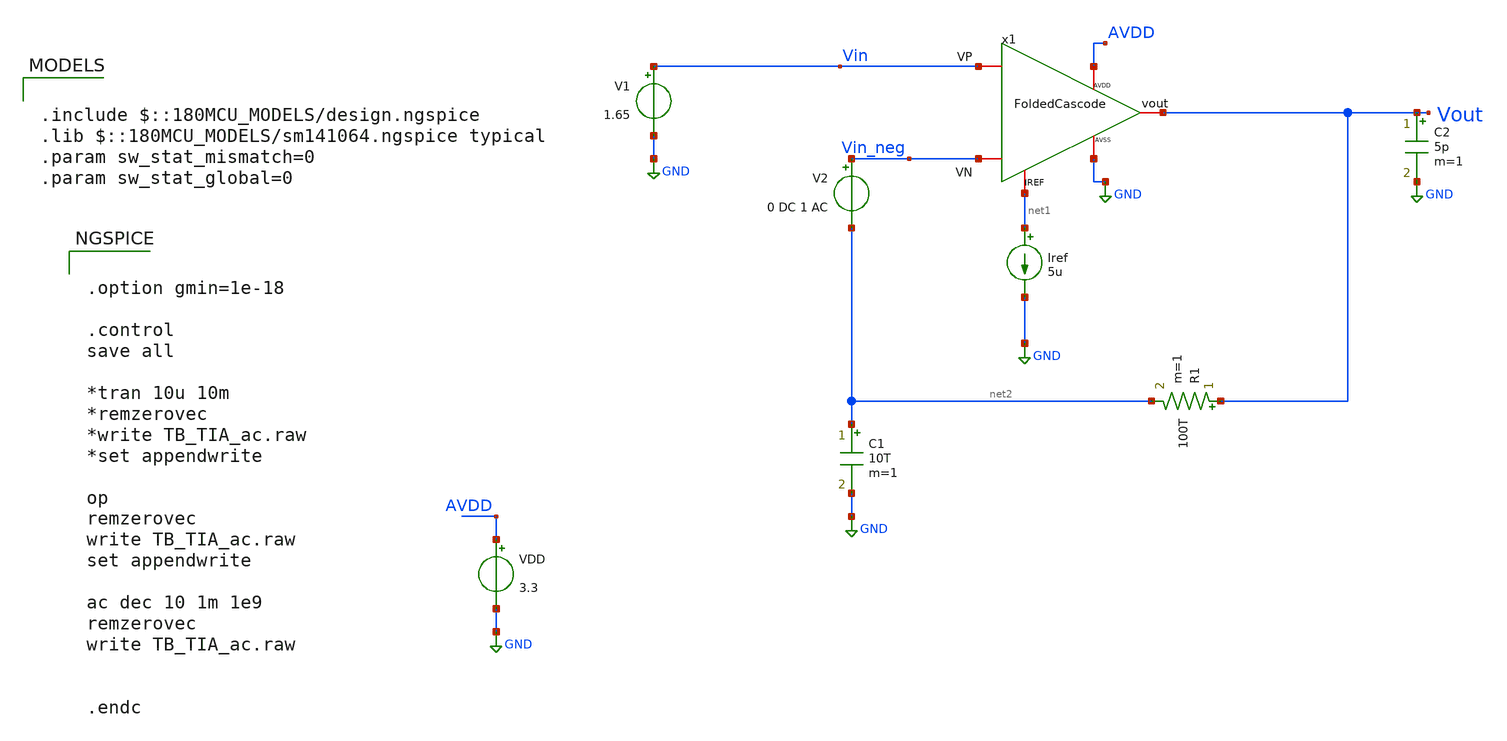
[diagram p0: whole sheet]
** sch_path: TIA_Filter/Folded/TB_Folded_ac.sch
**.subckt TB_Folded_ac
VDD AVDD GND 3.3
Iref net1 GND 5u
V1 Vin GND 1.65
C2 Vout GND 5p m=1
V2 Vin_neg net2 0 DC 1 AC
C1 net2 GND 10T m=1
R1 Vout net2 100T m=1
x1 Vin Vin_neg Vout net1 AVDD GND FoldedCascode
**** begin user architecture code

.include $::180MCU_MODELS/design.ngspice
.lib $::180MCU_MODELS/sm141064.ngspice typical
.param sw_stat_mismatch=0
.param sw_stat_global=0



.option gmin=1e-18

.control
save all

*tran 10u 10m
*remzerovec
*write TB_TIA_ac.raw
*set appendwrite

op
remzerovec
write TB_TIA_ac.raw
set appendwrite

ac dec 10 1m 1e9
remzerovec
write TB_TIA_ac.raw


.endc


**** end user architecture code
**.ends
.GLOBAL GND
.end
